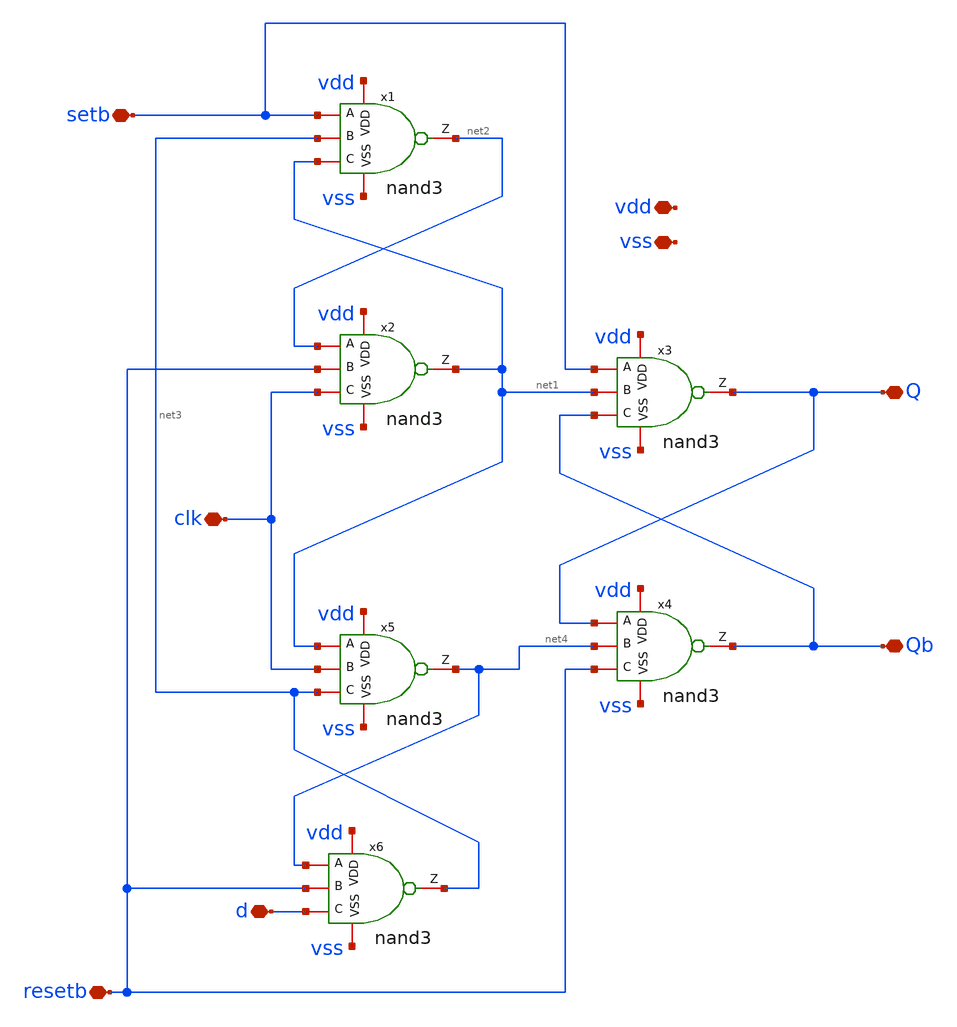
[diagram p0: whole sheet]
** sch_path: designs/comparator/final_magic/dffrs/dffrs.sch
**.subckt dffrs vdd vss Q Qb d clk resetb setb
*.iopin vdd
*.iopin vss
*.iopin Q
*.iopin Qb
*.iopin d
*.iopin clk
*.iopin resetb
*.iopin setb
x1 vdd net2 setb net3 net1 vss nand3
x2 vdd net1 net2 resetb clk vss nand3
x3 vdd Q setb net1 Qb vss nand3
x4 vdd Qb Q net4 resetb vss nand3
x5 vdd net4 net1 clk net3 vss nand3
x6 vdd net3 net4 resetb d vss nand3
**.ends
.end
